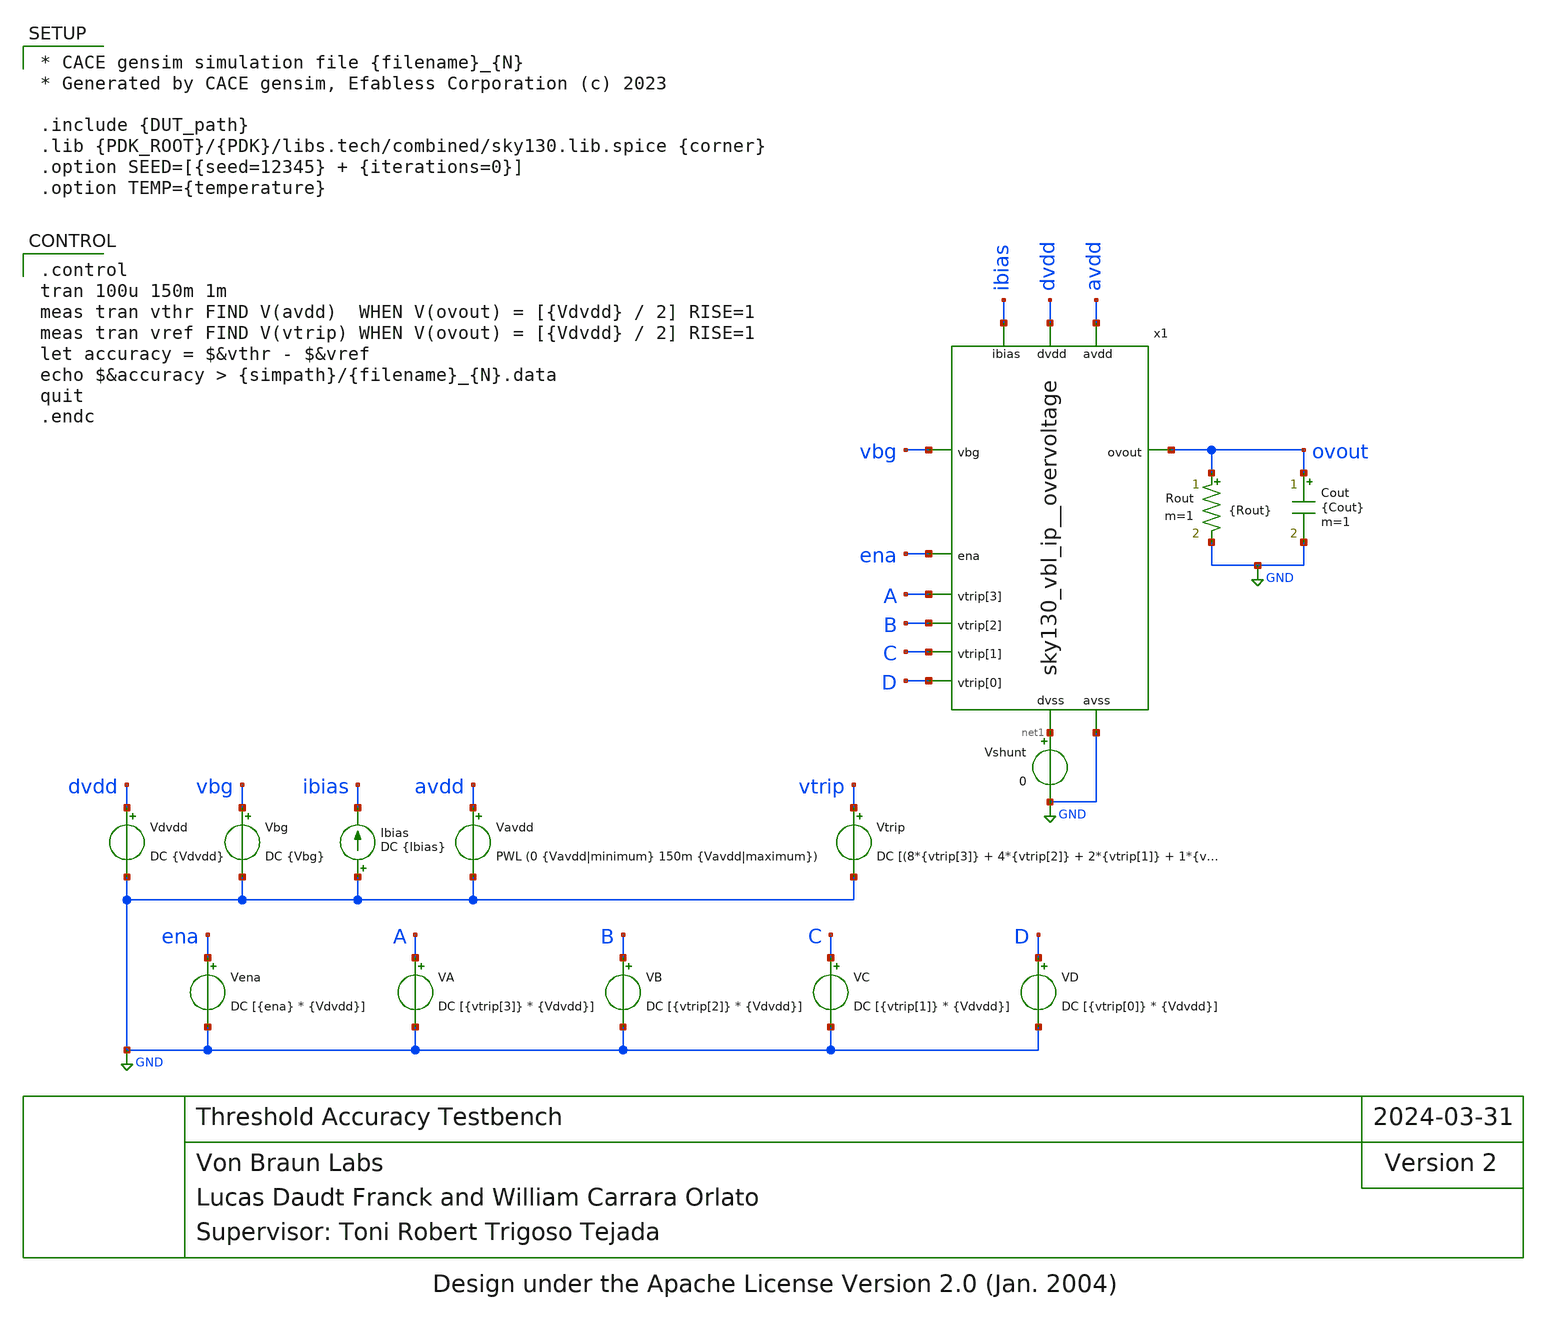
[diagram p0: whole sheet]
** sch_path: cace/tb_vacc.sch
* Design under the Apache License Version 2.0 (Jan. 2004)
**.subckt tb_vacc
Vavdd avdd GND PWL (0 {Vavdd|minimum} 150m {Vavdd|maximum})
Vdvdd dvdd GND DC {Vdvdd}
Vbg vbg GND DC {Vbg}
Ibias GND ibias DC {Ibias}
Vena ena GND DC [{ena} * {Vdvdd}]
VA A GND DC [{vtrip[3]} * {Vdvdd}]
VB B GND DC [{vtrip[2]} * {Vdvdd}]
VC C GND DC [{vtrip[1]} * {Vdvdd}]
VD D GND DC [{vtrip[0]} * {Vdvdd}]
Vtrip vtrip GND DC [(8*{vtrip[3]} + 4*{vtrip[2]} + 2*{vtrip[1]} + 1*{vtrip[0]})*0.14667 + 3.3]
Cout ovout GND {Cout} m=1
Rout ovout GND {Rout} m=1
x1 avdd dvdd ena A ibias B ovout vbg C D net1 GND sky130_vbl_ip__overvoltage
Vshunt net1 GND 0
**** begin user architecture code

* CACE gensim simulation file {filename}_{N}
* Generated by CACE gensim, Efabless Corporation (c) 2023

.include {DUT_path}
.lib {PDK_ROOT}/{PDK}/libs.tech/combined/sky130.lib.spice {corner}
.option SEED=[{seed=12345} + {iterations=0}]
.option TEMP={temperature}



.control
tran 100u 150m 1m
meas tran vthr FIND V(avdd)  WHEN V(ovout) = [{Vdvdd} / 2] RISE=1
meas tran vref FIND V(vtrip) WHEN V(ovout) = [{Vdvdd} / 2] RISE=1
let accuracy = $&vthr - $&vref
echo $&accuracy > {simpath}/{filename}_{N}.data
quit
.endc


**** end user architecture code
**.ends
.GLOBAL GND
.end
